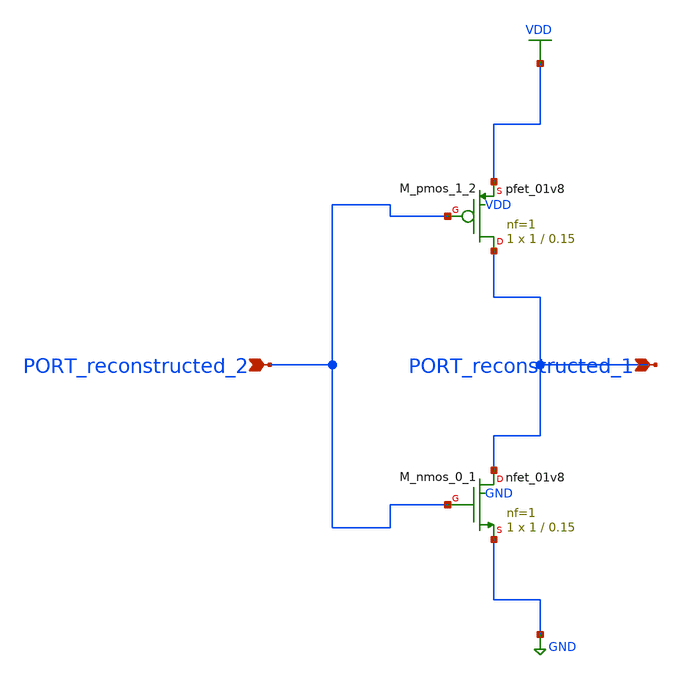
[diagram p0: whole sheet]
** sch_path: schematics/AMSNet/308.sch
**.subckt 308 PORT_reconstructed_2 PORT_reconstructed_1
*.ipin PORT_reconstructed_2
*.ipin PORT_reconstructed_1
XM_nmos_0_1 PORT_reconstructed_1 PORT_reconstructed_2 GND GND sky130_fd_pr__nfet_01v8 L=0.15 W=1 nf=1
+ ad='int((1 + 1)/2) * 1 / 1 * 0.29' as='int((1 + 2)/2) * 1 / 1 * 0.29' pd='2*int((1 + 1)/2) * (1 / 1 + 0.29)'
+ ps='2*int((1 + 2)/2) * (1 / 1 + 0.29)' nrd='0.29 / 1 ' nrs='0.29 / 1 ' sa=0 sb=0 sd=0 mult=1 m=1
XM_pmos_1_2 PORT_reconstructed_1 PORT_reconstructed_2 VDD VDD sky130_fd_pr__pfet_01v8 L=0.15 W=1 nf=1
+ ad='int((1 + 1)/2) * 1 / 1 * 0.29' as='int((1 + 2)/2) * 1 / 1 * 0.29' pd='2*int((1 + 1)/2) * (1 / 1 + 0.29)'
+ ps='2*int((1 + 2)/2) * (1 / 1 + 0.29)' nrd='0.29 / 1 ' nrs='0.29 / 1 ' sa=0 sb=0 sd=0 mult=1 m=1
**.ends
.GLOBAL GND
.GLOBAL VDD
.end
